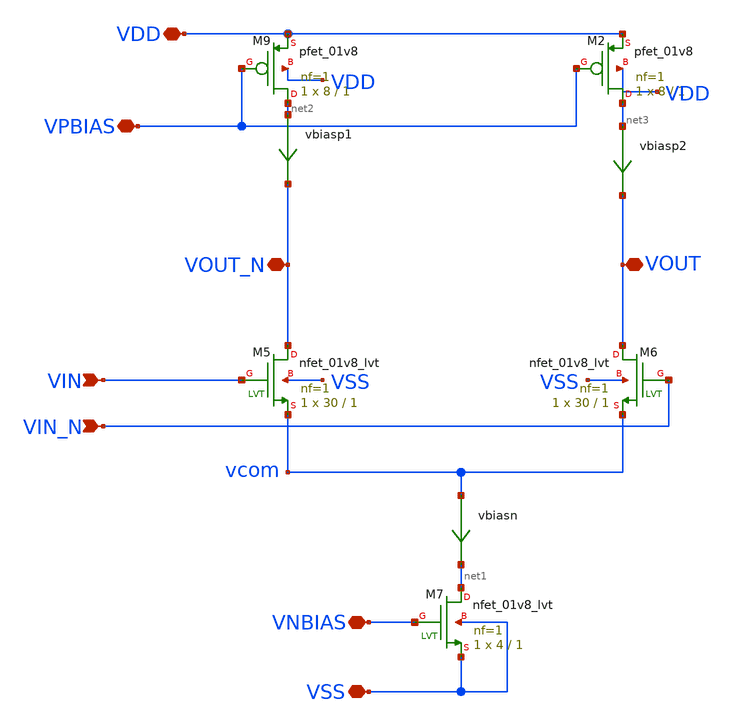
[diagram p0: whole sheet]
** sch_path: xschem/opamp1.sch
**.subckt opamp1 VSS VPBIAS VOUT_N VOUT VNBIAS VIN_N VIN VDD
*.iopin VSS
*.iopin VPBIAS
*.iopin VOUT_N
*.iopin VOUT
*.iopin VNBIAS
*.ipin VIN_N
*.ipin VIN
*.iopin VDD
XM5 VOUT_N VIN vcom VSS sky130_fd_pr__nfet_01v8_lvt L=1 W=30 nf=1 ad='int((nf+1)/2) * W/nf * 0.29' as='int((nf+2)/2) * W/nf * 0.29'
+ pd='2*int((nf+1)/2) * (W/nf + 0.29)' ps='2*int((nf+2)/2) * (W/nf + 0.29)' nrd='0.29 / W' nrs='0.29 / W'
+ sa=0 sb=0 sd=0 mult=1 m=1
XM6 VOUT VIN_N vcom VSS sky130_fd_pr__nfet_01v8_lvt L=1 W=30 nf=1 ad='int((nf+1)/2) * W/nf * 0.29' as='int((nf+2)/2) * W/nf * 0.29'
+ pd='2*int((nf+1)/2) * (W/nf + 0.29)' ps='2*int((nf+2)/2) * (W/nf + 0.29)' nrd='0.29 / W' nrs='0.29 / W'
+ sa=0 sb=0 sd=0 mult=1 m=1
XM7 net1 VNBIAS VSS VSS sky130_fd_pr__nfet_01v8_lvt L=1 W=4 nf=1 ad='int((nf+1)/2) * W/nf * 0.29' as='int((nf+2)/2) * W/nf * 0.29'
+ pd='2*int((nf+1)/2) * (W/nf + 0.29)' ps='2*int((nf+2)/2) * (W/nf + 0.29)' nrd='0.29 / W' nrs='0.29 / W'
+ sa=0 sb=0 sd=0 mult=1 m=1
vbiasn vcom net1 0
.save i(vbiasn)
XM9 net2 VPBIAS VDD VDD sky130_fd_pr__pfet_01v8 L=1 W=8 nf=1 ad='int((nf+1)/2) * W/nf * 0.29' as='int((nf+2)/2) * W/nf * 0.29'
+ pd='2*int((nf+1)/2) * (W/nf + 0.29)' ps='2*int((nf+2)/2) * (W/nf + 0.29)' nrd='0.29 / W' nrs='0.29 / W'
+ sa=0 sb=0 sd=0 mult=1 m=1
vbiasp1 net2 VOUT_N 0
.save i(vbiasp1)
XM2 net3 VPBIAS VDD VDD sky130_fd_pr__pfet_01v8 L=1 W=8 nf=1 ad='int((nf+1)/2) * W/nf * 0.29' as='int((nf+2)/2) * W/nf * 0.29'
+ pd='2*int((nf+1)/2) * (W/nf + 0.29)' ps='2*int((nf+2)/2) * (W/nf + 0.29)' nrd='0.29 / W' nrs='0.29 / W'
+ sa=0 sb=0 sd=0 mult=1 m=1
vbiasp2 net3 VOUT 0
.save i(vbiasp2)
**.ends
.end
